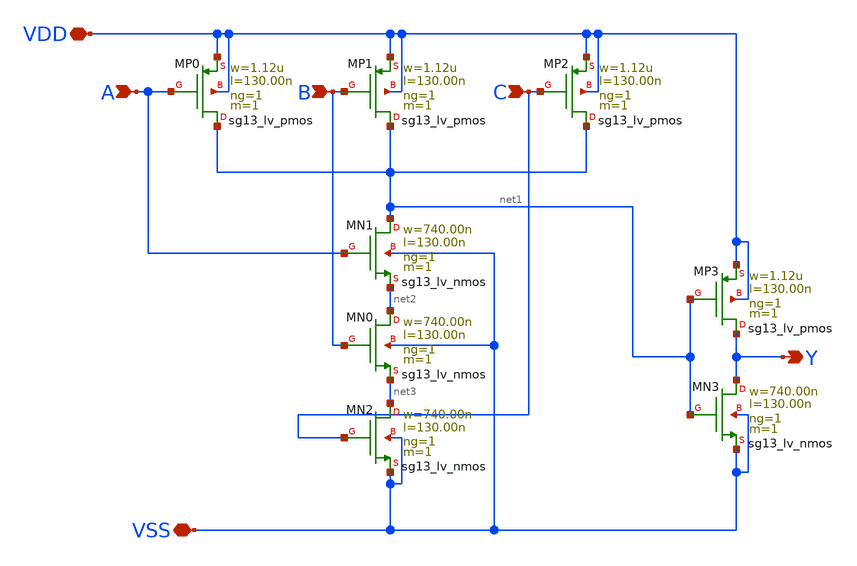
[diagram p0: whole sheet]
** sch_path: XSCHEM/AND_3.sch
**.subckt AND_3 A VDD VSS B C Y
*.ipin A
*.iopin VDD
*.iopin VSS
*.ipin B
*.ipin C
*.opin Y
XMN0 net2 B net3 VSS sg13_lv_nmos w=740.00n l=130.00n ng=1 m=1 mm_ok=1
XMP0 net1 A VDD VDD sg13_lv_pmos w=1.12u l=130.00n ng=1 m=1 mm_ok=1
XMN1 net1 A net2 VSS sg13_lv_nmos w=740.00n l=130.00n ng=1 m=1 mm_ok=1
XMN2 net3 C VSS VSS sg13_lv_nmos w=740.00n l=130.00n ng=1 m=1 mm_ok=1
XMP1 net1 B VDD VDD sg13_lv_pmos w=1.12u l=130.00n ng=1 m=1 mm_ok=1
XMP2 net1 C VDD VDD sg13_lv_pmos w=1.12u l=130.00n ng=1 m=1 mm_ok=1
XMN3 Y net1 VSS VSS sg13_lv_nmos w=740.00n l=130.00n ng=1 m=1 mm_ok=1
XMP3 Y net1 VDD VDD sg13_lv_pmos w=1.12u l=130.00n ng=1 m=1 mm_ok=1
**.ends
.end
